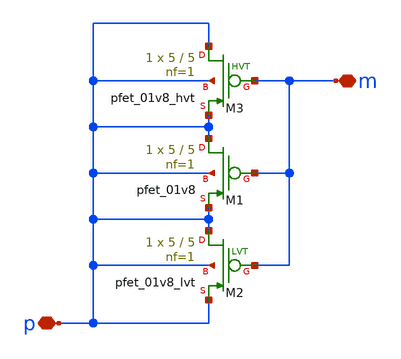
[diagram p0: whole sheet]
** sch_path: design/lc_oscillator_8ghz_varactor/oscillator_8ghz_varactor.sch
**.subckt oscillator_8ghz_varactor m p
*.iopin m
*.iopin p
XM1 p m p p sky130_fd_pr__pfet_01v8 L=5 W=5 nf=1 ad='int((nf+1)/2) * W/nf * 0.29' as='int((nf+2)/2) * W/nf * 0.29'
+ pd='2*int((nf+1)/2) * (W/nf + 0.29)' ps='2*int((nf+2)/2) * (W/nf + 0.29)' nrd='0.29 / W' nrs='0.29 / W'
+ sa=0 sb=0 sd=0 mult=1 m=1
XM2 p m p p sky130_fd_pr__pfet_01v8_lvt L=5 W=5 nf=1 ad='int((1 + 1)/2) * 5 / 1 * 0.29' as='int((1 + 2)/2) * 5 / 1 * 0.29'
+ pd='2*int((1 + 1)/2) * (5 / 1 + 0.29)' ps='2*int((1 + 2)/2) * (5 / 1 + 0.29)' nrd='0.29 / 5 ' nrs='0.29 / 5 '
+ sa=0 sb=0 sd=0 mult=1 m=1
XM3 p m p p sky130_fd_pr__pfet_01v8_hvt L=5 W=5 nf=1 ad='int((1 + 1)/2) * 5 / 1 * 0.29' as='int((1 + 2)/2) * 5 / 1 * 0.29'
+ pd='2*int((1 + 1)/2) * (5 / 1 + 0.29)' ps='2*int((1 + 2)/2) * (5 / 1 + 0.29)' nrd='0.29 / 5 ' nrs='0.29 / 5 '
+ sa=0 sb=0 sd=0 mult=1 m=1
**.ends
.end
